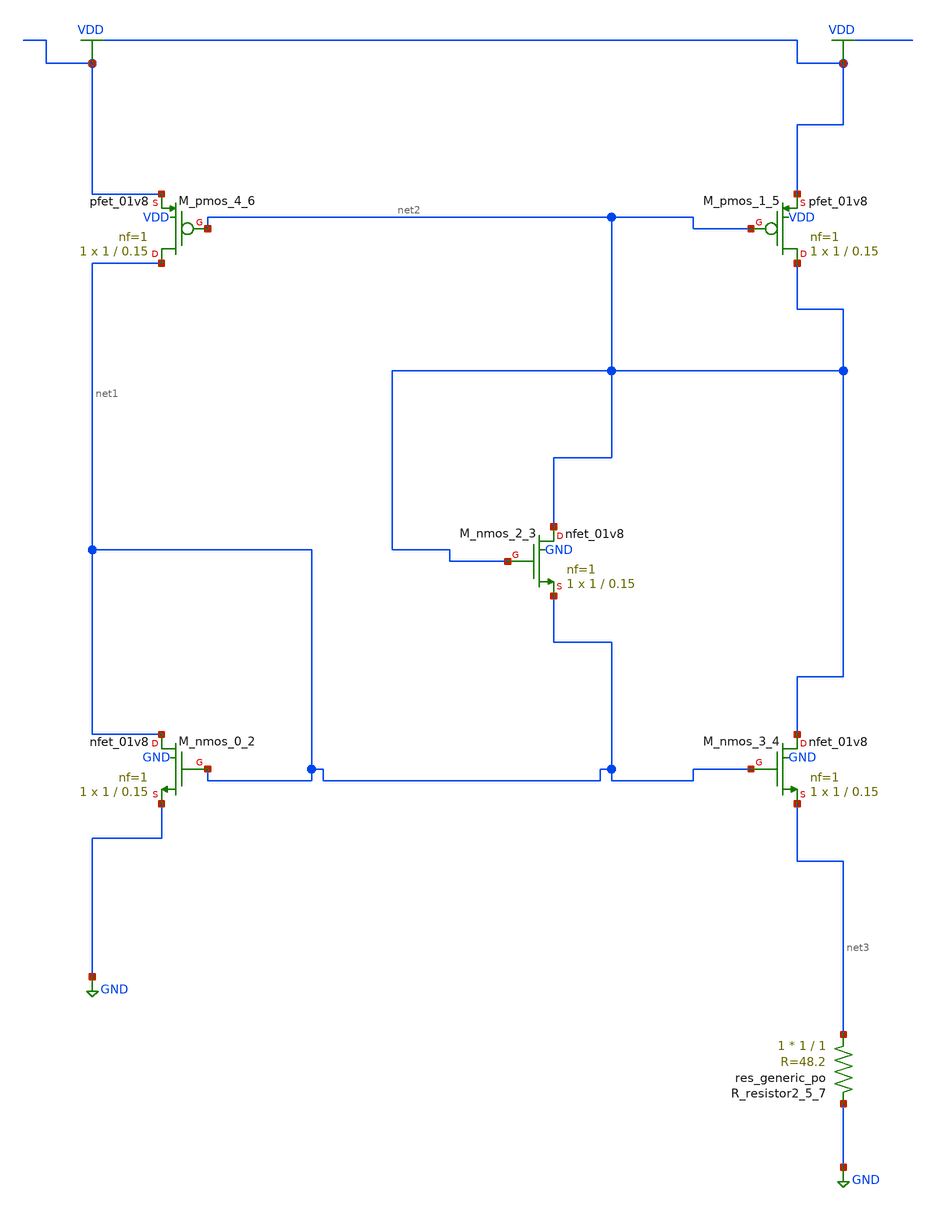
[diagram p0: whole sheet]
** sch_path: schematics/AMSNet/765.sch
**.subckt 765
XM_nmos_0_2 net1 net1 GND GND sky130_fd_pr__nfet_01v8 L=0.15 W=1 nf=1 ad='int((1 + 1)/2) * 1 / 1 * 0.29'
+ as='int((1 + 2)/2) * 1 / 1 * 0.29' pd='2*int((1 + 1)/2) * (1 / 1 + 0.29)' ps='2*int((1 + 2)/2) * (1 / 1 + 0.29)'
+ nrd='0.29 / 1 ' nrs='0.29 / 1 ' sa=0 sb=0 sd=0 mult=1 m=1
XM_nmos_2_3 net2 net2 net1 GND sky130_fd_pr__nfet_01v8 L=0.15 W=1 nf=1 ad='int((1 + 1)/2) * 1 / 1 * 0.29'
+ as='int((1 + 2)/2) * 1 / 1 * 0.29' pd='2*int((1 + 1)/2) * (1 / 1 + 0.29)' ps='2*int((1 + 2)/2) * (1 / 1 + 0.29)'
+ nrd='0.29 / 1 ' nrs='0.29 / 1 ' sa=0 sb=0 sd=0 mult=1 m=1
XM_nmos_3_4 net2 net1 net3 GND sky130_fd_pr__nfet_01v8 L=0.15 W=1 nf=1 ad='int((1 + 1)/2) * 1 / 1 * 0.29'
+ as='int((1 + 2)/2) * 1 / 1 * 0.29' pd='2*int((1 + 1)/2) * (1 / 1 + 0.29)' ps='2*int((1 + 2)/2) * (1 / 1 + 0.29)'
+ nrd='0.29 / 1 ' nrs='0.29 / 1 ' sa=0 sb=0 sd=0 mult=1 m=1
XM_pmos_1_5 net2 net2 VDD VDD sky130_fd_pr__pfet_01v8 L=0.15 W=1 nf=1 ad='int((1 + 1)/2) * 1 / 1 * 0.29'
+ as='int((1 + 2)/2) * 1 / 1 * 0.29' pd='2*int((1 + 1)/2) * (1 / 1 + 0.29)' ps='2*int((1 + 2)/2) * (1 / 1 + 0.29)'
+ nrd='0.29 / 1 ' nrs='0.29 / 1 ' sa=0 sb=0 sd=0 mult=1 m=1
XM_pmos_4_6 net1 net2 VDD VDD sky130_fd_pr__pfet_01v8 L=0.15 W=1 nf=1 ad='int((1 + 1)/2) * 1 / 1 * 0.29'
+ as='int((1 + 2)/2) * 1 / 1 * 0.29' pd='2*int((1 + 1)/2) * (1 / 1 + 0.29)' ps='2*int((1 + 2)/2) * (1 / 1 + 0.29)'
+ nrd='0.29 / 1 ' nrs='0.29 / 1 ' sa=0 sb=0 sd=0 mult=1 m=1
XR_resistor2_5_7 net3 GND sky130_fd_pr__res_generic_po W=1 L=1 m=1
**.ends
.GLOBAL GND
.GLOBAL VDD
.end
